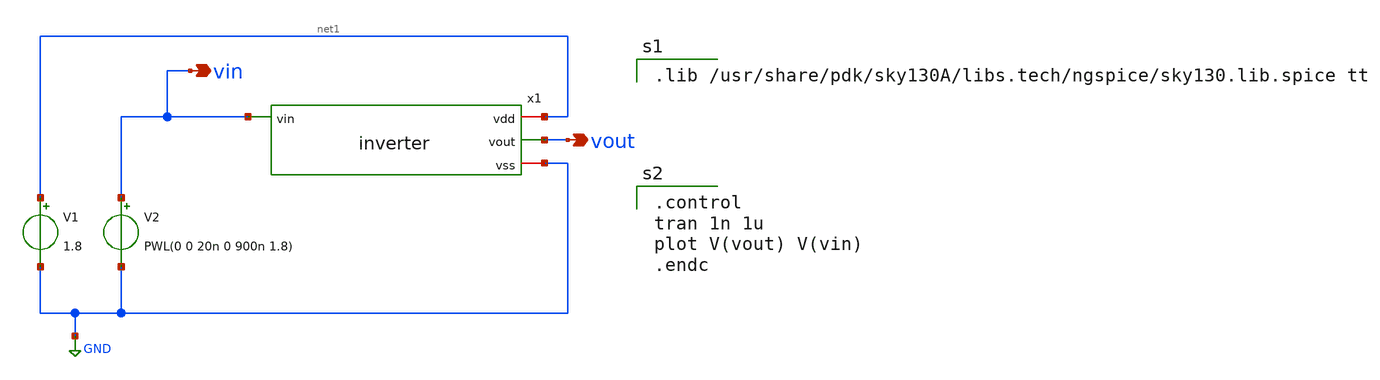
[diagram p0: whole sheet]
** sch_path: inverter/xschem/tb_inverter.sch
**.subckt tb_inverter vin vout
*.opin vin
*.opin vout
x1 net1 vin vout GND inverter
V1 net1 GND 1.8
V2 vin GND PWL(0 0 20n 0 900n 1.8)
**** begin user architecture code

.lib /usr/share/pdk/sky130A/libs.tech/ngspice/sky130.lib.spice tt


.control
tran 1n 1u
plot V(vout) V(vin)
.endc

**** end user architecture code
**.ends

* expanding   symbol:  inverter.sym # of pins=4
** sym_path: inverter/xschem/inverter.sym
** sch_path: inverter/xschem/inverter.sch
.subckt inverter vdd vin vout vss
*.ipin vin
*.iopin vdd
*.iopin vss
*.opin vout
XM3 vout vin vss vss sky130_fd_pr__nfet_01v8 L=0.18 W=4.5 nf=3 ad='int((nf+1)/2) * W/nf * 0.29' as='int((nf+2)/2) * W/nf * 0.29'
+ pd='2*int((nf+1)/2) * (W/nf + 0.29)' ps='2*int((nf+2)/2) * (W/nf + 0.29)' nrd='0.29 / W' nrs='0.29 / W'
+ sa=0 sb=0 sd=0 mult=1 m=1
XM1 vout vin vdd vdd sky130_fd_pr__pfet_01v8 L=0.18 W=3 nf=3 ad='int((nf+1)/2) * W/nf * 0.29' as='int((nf+2)/2) * W/nf * 0.29'
+ pd='2*int((nf+1)/2) * (W/nf + 0.29)' ps='2*int((nf+2)/2) * (W/nf + 0.29)' nrd='0.29 / W' nrs='0.29 / W'
+ sa=0 sb=0 sd=0 mult=1 m=1
.ends

.GLOBAL GND
.end
